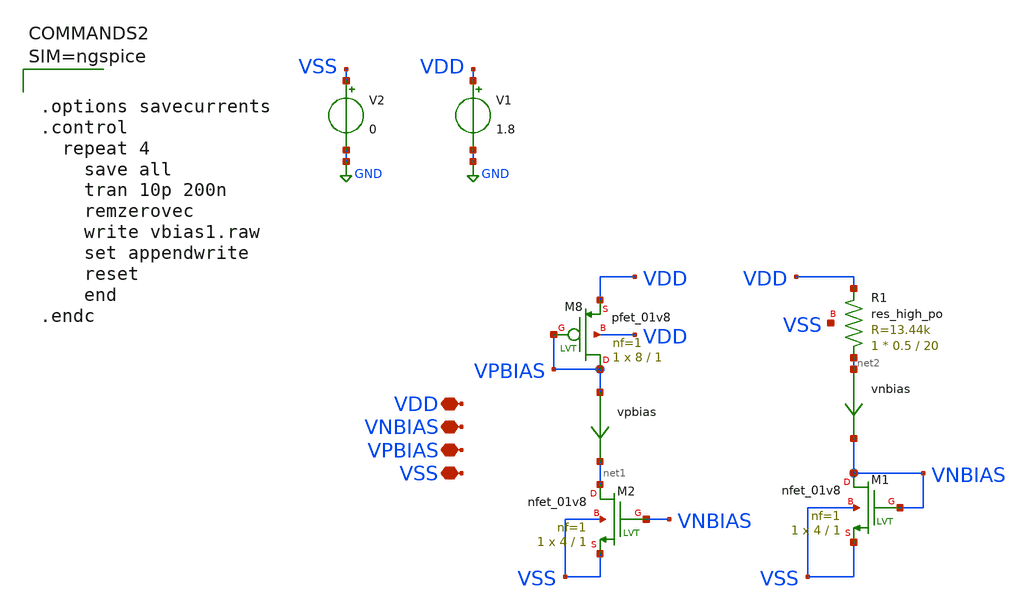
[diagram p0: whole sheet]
** sch_path: tt_um_emilian_rf_playground/xschem/tb_vbias1.sch
**.subckt tb_vbias1 VSS VPBIAS VNBIAS VDD
*.iopin VSS
*.iopin VPBIAS
*.iopin VNBIAS
*.iopin VDD
XM8 VPBIAS VPBIAS VDD VDD sky130_fd_pr__pfet_01v8 L=1 W=8 nf=1 ad='int((nf+1)/2) * W/nf * 0.29' as='int((nf+2)/2) * W/nf * 0.29'
+ pd='2*int((nf+1)/2) * (W/nf + 0.29)' ps='2*int((nf+2)/2) * (W/nf + 0.29)' nrd='0.29 / W' nrs='0.29 / W'
+ sa=0 sb=0 sd=0 mult=1 m=1
XR1 net2 VDD VSS sky130_fd_pr__res_high_po W=0.5 L=20 mult=1 m=1
V1 VDD GND 1.8
V2 VSS GND 0
vnbias net2 VNBIAS 0
.save i(vnbias)
vpbias VPBIAS net1 0
.save i(vpbias)
XM1 VNBIAS VNBIAS VSS VSS sky130_fd_pr__nfet_01v8 L=1 W=4 nf=1 ad='int((nf+1)/2) * W/nf * 0.29' as='int((nf+2)/2) * W/nf * 0.29'
+ pd='2*int((nf+1)/2) * (W/nf + 0.29)' ps='2*int((nf+2)/2) * (W/nf + 0.29)' nrd='0.29 / W' nrs='0.29 / W'
+ sa=0 sb=0 sd=0 mult=1 m=1
XM2 net1 VNBIAS VSS VSS sky130_fd_pr__nfet_01v8 L=1 W=4 nf=1 ad='int((nf+1)/2) * W/nf * 0.29' as='int((nf+2)/2) * W/nf * 0.29'
+ pd='2*int((nf+1)/2) * (W/nf + 0.29)' ps='2*int((nf+2)/2) * (W/nf + 0.29)' nrd='0.29 / W' nrs='0.29 / W'
+ sa=0 sb=0 sd=0 mult=1 m=1
**** begin user architecture code

** opencircuitdesign pdks install
.lib $::SKYWATER_MODELS/sky130.lib.spice tt_mm





.options savecurrents
.control
  repeat 4
    save all
    tran 10p 200n
    remzerovec
    write vbias1.raw
    set appendwrite
    reset
    end
.endc



**** end user architecture code
**.ends
.GLOBAL GND
.end
